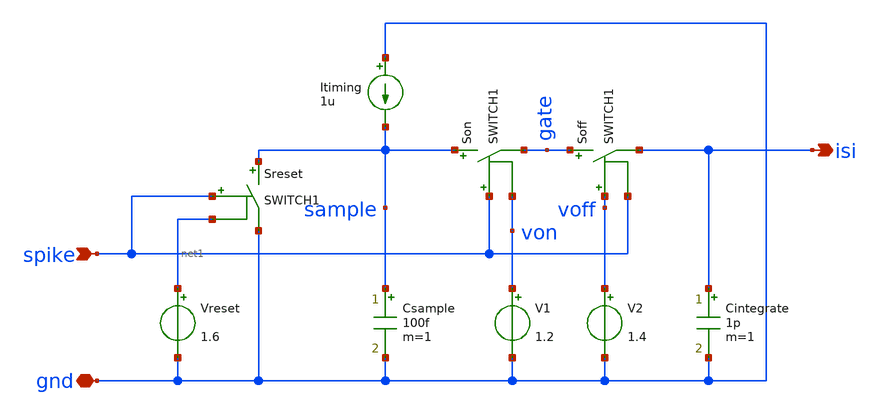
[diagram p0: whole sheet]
** sch_path: playground/InterServicesIntelligence.sch
**.subckt InterServicesIntelligence gnd spike isi
*.iopin gnd
*.ipin spike
*.opin isi
Csample sample gnd 100f m=1
Itiming gnd sample 1u
Son sample gate spike von SWITCH1
Sreset sample gnd spike net1 SWITCH1
Cintegrate isi gnd 1p m=1
V1 von gnd 1.2
Vreset net1 gnd 1.6
Soff gate isi voff spike SWITCH1
V2 voff gnd 1.4
**.ends
.end
